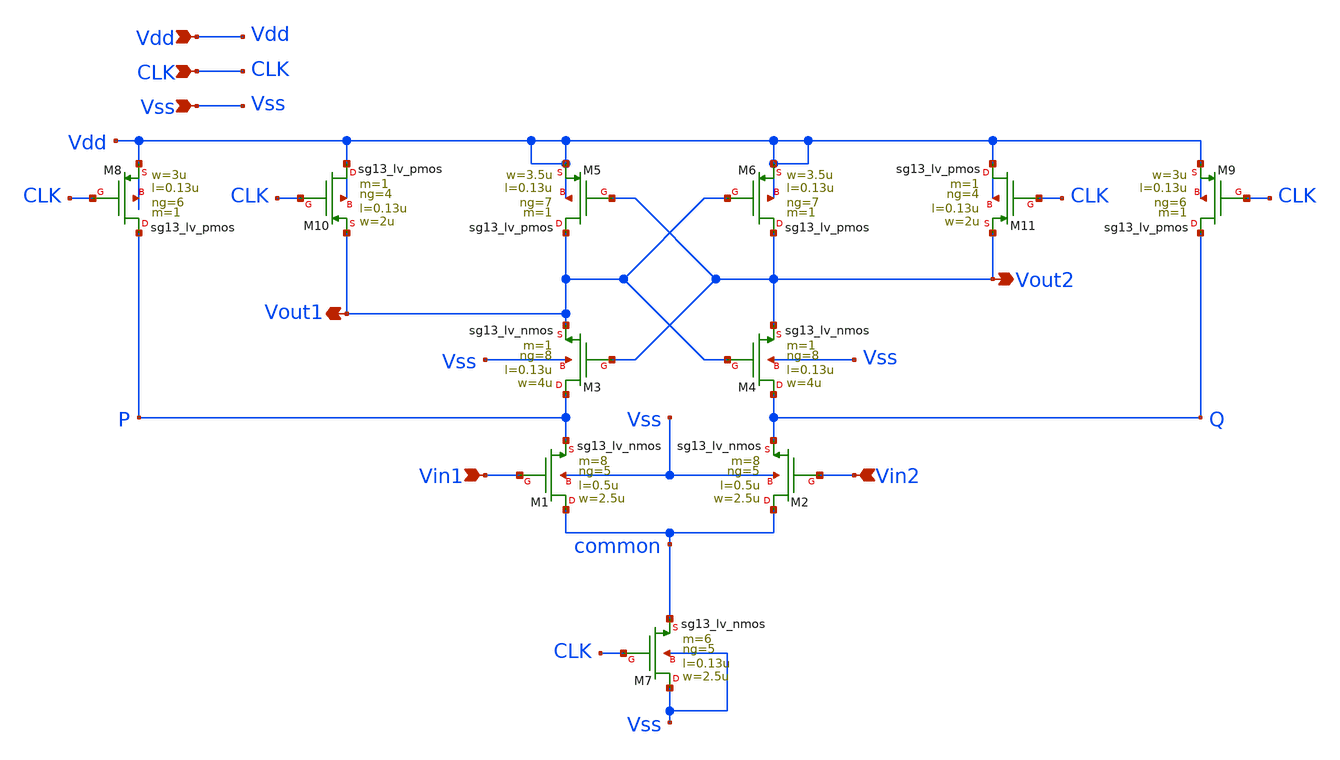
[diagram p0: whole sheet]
** sch_path: xschem/sch/strongarm_dimensionado.sch
**.subckt strongarm_dimensionado Vout2 Vout1 Vin1 Vin2 CLK Vss Vdd
*.opin Vout2
*.opin Vout1
*.ipin Vin1
*.ipin Vin2
*.ipin CLK
*.ipin Vss
*.ipin Vdd
XM1 common Vin1 P Vss sg13_lv_nmos w=2.5u l=0.5u ng=5 m=8 mm_ok=1
XM2 common Vin2 Q Vss sg13_lv_nmos w=2.5u l=0.5u ng=5 m=8 mm_ok=1
XM3 P Vout2 Vout1 Vss sg13_lv_nmos w=4u l=0.13u ng=8 m=1 mm_ok=1
XM4 Q Vout1 Vout2 Vss sg13_lv_nmos w=4u l=0.13u ng=8 m=1 mm_ok=1
XM6 Vout2 Vout1 Vdd Vdd sg13_lv_pmos w=3.5u l=0.13u ng=7 m=1 mm_ok=1
XM5 Vout1 Vout2 Vdd Vdd sg13_lv_pmos w=3.5u l=0.13u ng=7 m=1 mm_ok=1
XM7 Vss CLK common Vss sg13_lv_nmos w=2.5u l=0.13u ng=5 m=6 mm_ok=1
XM8 P CLK Vdd Vdd sg13_lv_pmos w=3u l=0.13u ng=6 m=1 mm_ok=1
XM9 Q CLK Vdd Vdd sg13_lv_pmos w=3u l=0.13u ng=6 m=1 mm_ok=1
XM11 Vdd CLK Vout2 Vdd sg13_lv_pmos w=2u l=0.13u ng=4 m=1 mm_ok=1
XM10 Vdd CLK Vout1 Vdd sg13_lv_pmos w=2u l=0.13u ng=4 m=1 mm_ok=1
**.ends
.end
